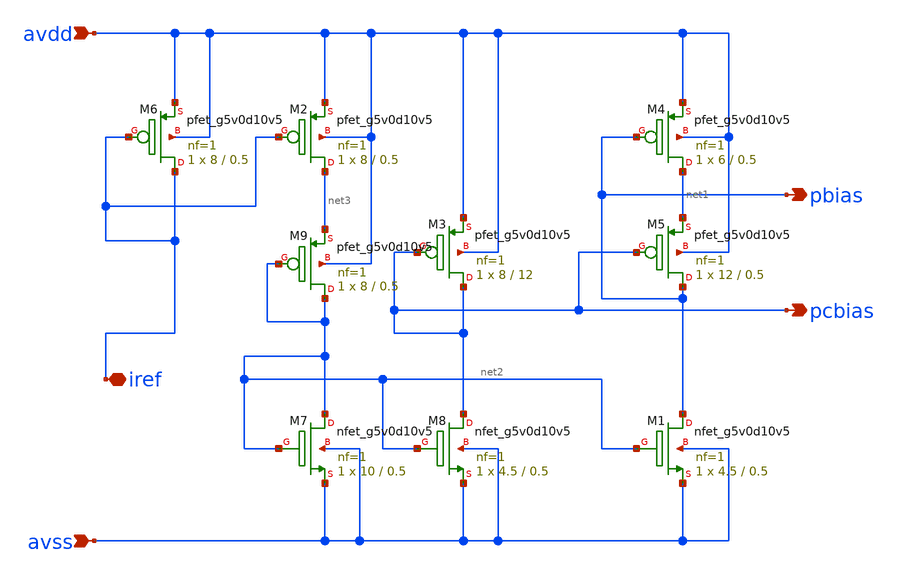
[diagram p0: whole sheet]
** sch_path: xschem/p_ibias.sch
**.subckt p_ibias avdd iref avss pbias pcbias
*.ipin avdd
*.iopin iref
*.ipin avss
*.opin pbias
*.opin pcbias
XM3 pcbias pcbias avdd avdd sky130_fd_pr__pfet_g5v0d10v5 L=12 W=8 nf=1 ad='int((nf+1)/2) * W/nf * 0.29'
+ as='int((nf+2)/2) * W/nf * 0.29' pd='2*int((nf+1)/2) * (W/nf + 0.29)' ps='2*int((nf+2)/2) * (W/nf + 0.29)'
+ nrd='0.29 / W' nrs='0.29 / W' sa=0 sb=0 sd=0 mult=1 m=1
XM4 net1 pbias avdd avdd sky130_fd_pr__pfet_g5v0d10v5 L=0.5 W=6 nf=1 ad='int((nf+1)/2) * W/nf * 0.29'
+ as='int((nf+2)/2) * W/nf * 0.29' pd='2*int((nf+1)/2) * (W/nf + 0.29)' ps='2*int((nf+2)/2) * (W/nf + 0.29)'
+ nrd='0.29 / W' nrs='0.29 / W' sa=0 sb=0 sd=0 mult=1 m=1
XM5 pbias pcbias net1 avdd sky130_fd_pr__pfet_g5v0d10v5 L=0.5 W=12 nf=1 ad='int((nf+1)/2) * W/nf * 0.29'
+ as='int((nf+2)/2) * W/nf * 0.29' pd='2*int((nf+1)/2) * (W/nf + 0.29)' ps='2*int((nf+2)/2) * (W/nf + 0.29)'
+ nrd='0.29 / W' nrs='0.29 / W' sa=0 sb=0 sd=0 mult=1 m=1
XM6 iref iref avdd avdd sky130_fd_pr__pfet_g5v0d10v5 L=0.5 W=8 nf=1 ad='int((nf+1)/2) * W/nf * 0.29'
+ as='int((nf+2)/2) * W/nf * 0.29' pd='2*int((nf+1)/2) * (W/nf + 0.29)' ps='2*int((nf+2)/2) * (W/nf + 0.29)'
+ nrd='0.29 / W' nrs='0.29 / W' sa=0 sb=0 sd=0 mult=1 m=1
XM1 pbias net2 avss avss sky130_fd_pr__nfet_g5v0d10v5 L=0.5 W=4.5 nf=1 ad='int((nf+1)/2) * W/nf * 0.29'
+ as='int((nf+2)/2) * W/nf * 0.29' pd='2*int((nf+1)/2) * (W/nf + 0.29)' ps='2*int((nf+2)/2) * (W/nf + 0.29)'
+ nrd='0.29 / W' nrs='0.29 / W' sa=0 sb=0 sd=0 mult=1 m=1
XM2 net3 iref avdd avdd sky130_fd_pr__pfet_g5v0d10v5 L=0.5 W=8 nf=1 ad='int((nf+1)/2) * W/nf * 0.29'
+ as='int((nf+2)/2) * W/nf * 0.29' pd='2*int((nf+1)/2) * (W/nf + 0.29)' ps='2*int((nf+2)/2) * (W/nf + 0.29)'
+ nrd='0.29 / W' nrs='0.29 / W' sa=0 sb=0 sd=0 mult=1 m=1
XM7 net2 net2 avss avss sky130_fd_pr__nfet_g5v0d10v5 L=0.5 W=10 nf=1 ad='int((nf+1)/2) * W/nf * 0.29'
+ as='int((nf+2)/2) * W/nf * 0.29' pd='2*int((nf+1)/2) * (W/nf + 0.29)' ps='2*int((nf+2)/2) * (W/nf + 0.29)'
+ nrd='0.29 / W' nrs='0.29 / W' sa=0 sb=0 sd=0 mult=1 m=1
XM8 pcbias net2 avss avss sky130_fd_pr__nfet_g5v0d10v5 L=0.5 W=4.5 nf=1 ad='int((nf+1)/2) * W/nf * 0.29'
+ as='int((nf+2)/2) * W/nf * 0.29' pd='2*int((nf+1)/2) * (W/nf + 0.29)' ps='2*int((nf+2)/2) * (W/nf + 0.29)'
+ nrd='0.29 / W' nrs='0.29 / W' sa=0 sb=0 sd=0 mult=1 m=1
XM9 net2 net2 net3 avdd sky130_fd_pr__pfet_g5v0d10v5 L=0.5 W=8 nf=1 ad='int((nf+1)/2) * W/nf * 0.29'
+ as='int((nf+2)/2) * W/nf * 0.29' pd='2*int((nf+1)/2) * (W/nf + 0.29)' ps='2*int((nf+2)/2) * (W/nf + 0.29)'
+ nrd='0.29 / W' nrs='0.29 / W' sa=0 sb=0 sd=0 mult=1 m=1
**.ends
.end
